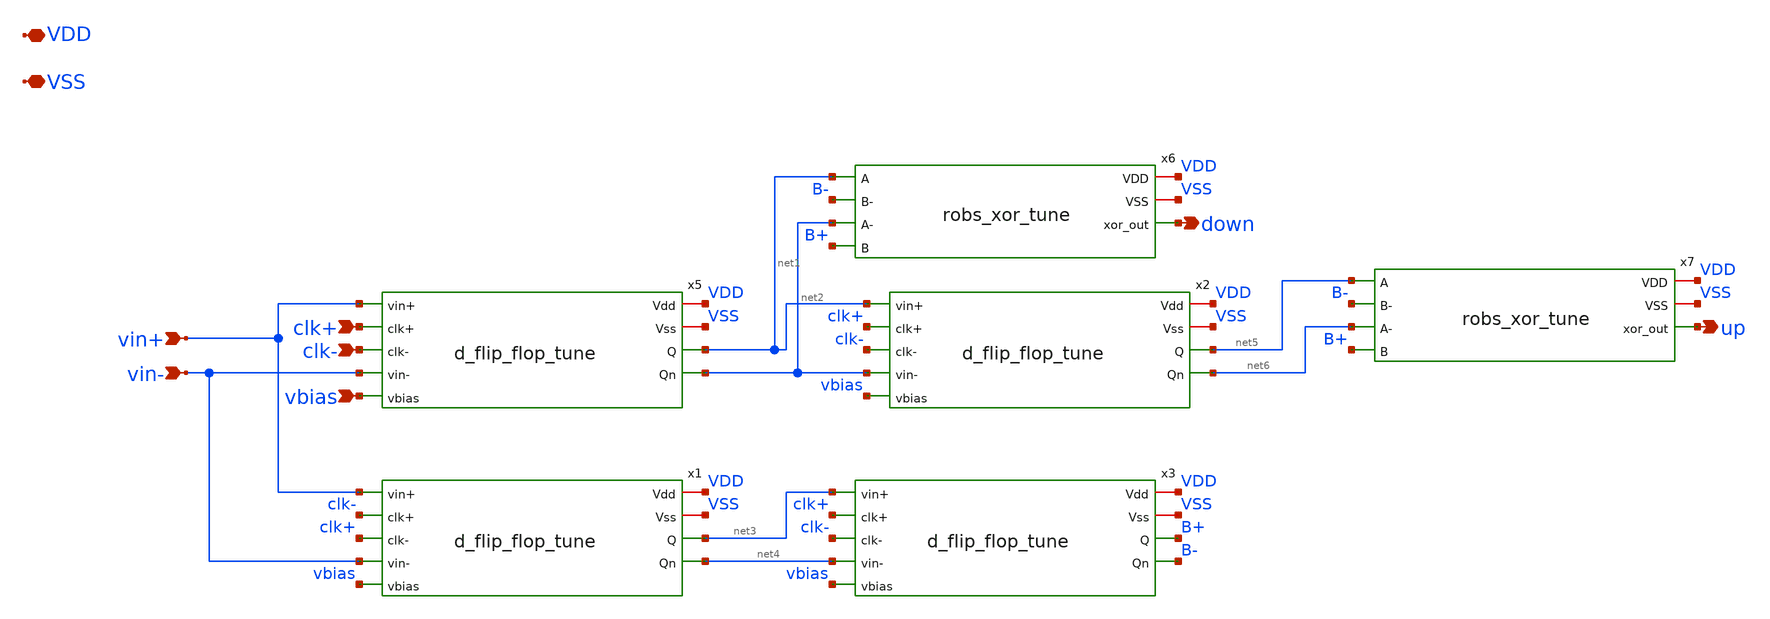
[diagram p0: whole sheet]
** sch_path: xschem/tuning/alexander_phase_detector_tune.sch
**.subckt alexander_phase_detector_tune down up vin+ vin- clk+ clk- vbias VDD VSS
*.opin down
*.opin up
*.ipin vin+
*.ipin vin-
*.ipin clk+
*.ipin clk-
*.ipin vbias
*.iopin VDD
*.iopin VSS
x6 net1 VDD B- VSS down net2 B+ robs_xor_tune
x7 net5 VDD B- VSS up net6 B+ robs_xor_tune
x5 VDD VSS net1 net2 vin+ clk+ clk- vin- vbias d_flip_flop_tune
x1 VDD VSS net3 net4 vin+ clk- clk+ vin- vbias d_flip_flop_tune
x2 VDD VSS net5 net6 net1 clk+ clk- net2 vbias d_flip_flop_tune
x3 VDD VSS B+ B- net3 clk+ clk- net4 vbias d_flip_flop_tune
**.ends

* expanding   symbol:  robs_xor_tune.sym # of pins=7
** sym_path: xschem/tuning/robs_xor_tune.sym
** sch_path: xschem/tuning/robs_xor_tune.sch
.subckt robs_xor_tune A VDD B- VSS xor_out A- B
*.opin xor_out
*.ipin A
*.ipin B-
*.ipin A-
*.ipin B
*.iopin VDD
*.iopin VSS
XM5 net1 A VDD VDD sky130_fd_pr__pfet_01v8 L=0.15 W=2 nf=1 ad='int((nf+1)/2) * W/nf * 0.29' as='int((nf+2)/2) * W/nf * 0.29'
+ pd='2*int((nf+1)/2) * (W/nf + 0.29)' ps='2*int((nf+2)/2) * (W/nf + 0.29)' nrd='0.29 / W' nrs='0.29 / W'
+ sa=0 sb=0 sd=0 mult=1 m=1
XM6 xor_out A- net3 VSS sky130_fd_pr__nfet_01v8 L=0.15 W=2 nf=1 ad='int((nf+1)/2) * W/nf * 0.29' as='int((nf+2)/2) * W/nf * 0.29'
+ pd='2*int((nf+1)/2) * (W/nf + 0.29)' ps='2*int((nf+2)/2) * (W/nf + 0.29)' nrd='0.29 / W' nrs='0.29 / W'
+ sa=0 sb=0 sd=0 mult=1 m=1
XM1 xor_out B- net1 VDD sky130_fd_pr__pfet_01v8 L=0.15 W=2 nf=1 ad='int((nf+1)/2) * W/nf * 0.29' as='int((nf+2)/2) * W/nf * 0.29'
+ pd='2*int((nf+1)/2) * (W/nf + 0.29)' ps='2*int((nf+2)/2) * (W/nf + 0.29)' nrd='0.29 / W' nrs='0.29 / W'
+ sa=0 sb=0 sd=0 mult=1 m=1
XM2 net2 A- VDD VDD sky130_fd_pr__pfet_01v8 L=0.15 W=2 nf=1 ad='int((nf+1)/2) * W/nf * 0.29' as='int((nf+2)/2) * W/nf * 0.29'
+ pd='2*int((nf+1)/2) * (W/nf + 0.29)' ps='2*int((nf+2)/2) * (W/nf + 0.29)' nrd='0.29 / W' nrs='0.29 / W'
+ sa=0 sb=0 sd=0 mult=1 m=1
XM3 xor_out B net2 VDD sky130_fd_pr__pfet_01v8 L=0.15 W=2 nf=1 ad='int((nf+1)/2) * W/nf * 0.29' as='int((nf+2)/2) * W/nf * 0.29'
+ pd='2*int((nf+1)/2) * (W/nf + 0.29)' ps='2*int((nf+2)/2) * (W/nf + 0.29)' nrd='0.29 / W' nrs='0.29 / W'
+ sa=0 sb=0 sd=0 mult=1 m=1
XM4 net3 B- VSS VSS sky130_fd_pr__nfet_01v8 L=0.15 W=2 nf=1 ad='int((nf+1)/2) * W/nf * 0.29' as='int((nf+2)/2) * W/nf * 0.29'
+ pd='2*int((nf+1)/2) * (W/nf + 0.29)' ps='2*int((nf+2)/2) * (W/nf + 0.29)' nrd='0.29 / W' nrs='0.29 / W'
+ sa=0 sb=0 sd=0 mult=1 m=1
XM7 xor_out A net4 VSS sky130_fd_pr__nfet_01v8 L=0.15 W=2 nf=1 ad='int((nf+1)/2) * W/nf * 0.29' as='int((nf+2)/2) * W/nf * 0.29'
+ pd='2*int((nf+1)/2) * (W/nf + 0.29)' ps='2*int((nf+2)/2) * (W/nf + 0.29)' nrd='0.29 / W' nrs='0.29 / W'
+ sa=0 sb=0 sd=0 mult=1 m=1
XM8 net4 B VSS VSS sky130_fd_pr__nfet_01v8 L=0.15 W=2 nf=1 ad='int((nf+1)/2) * W/nf * 0.29' as='int((nf+2)/2) * W/nf * 0.29'
+ pd='2*int((nf+1)/2) * (W/nf + 0.29)' ps='2*int((nf+2)/2) * (W/nf + 0.29)' nrd='0.29 / W' nrs='0.29 / W'
+ sa=0 sb=0 sd=0 mult=1 m=1
.ends


* expanding   symbol:  d_flip_flop_tune.sym # of pins=9
** sym_path: xschem/tuning/d_flip_flop_tune.sym
** sch_path: xschem/tuning/d_flip_flop_tune.sch
.subckt d_flip_flop_tune Vdd Vss Q Qn vin+ clk+ clk- vin- vbias
*.opin Qn
*.opin Q
*.ipin vin+
*.ipin vin-
*.ipin clk+
*.ipin clk-
*.ipin vbias
*.iopin Vdd
*.iopin Vss
x1 net1 net2 vin+ vin- Vdd Vss clk- clk+ vbias d_latch_tune
x2 Q Qn net1 net2 Vdd Vss clk+ clk- vbias d_latch_tune
.ends


* expanding   symbol:  d_latch_tune.sym # of pins=9
** sym_path: xschem/tuning/d_latch_tune.sym
** sch_path: xschem/tuning/d_latch_tune.sch
.subckt d_latch_tune vout+ vout- vin+ vin- VDD VSS clk+ clk- vbias
*.iopin VDD
*.iopin VSS
*.ipin vin+
*.ipin clk-
*.ipin vbias
*.opin vout+
*.ipin clk+
*.opin vout-
*.ipin vin-
XM1 net1 vin+ net3 VSS sky130_fd_pr__nfet_01v8 L=0.15 W=5 nf=1 ad='int((nf+1)/2) * W/nf * 0.29' as='int((nf+2)/2) * W/nf * 0.29'
+ pd='2*int((nf+1)/2) * (W/nf + 0.29)' ps='2*int((nf+2)/2) * (W/nf + 0.29)' nrd='0.29 / W' nrs='0.29 / W'
+ sa=0 sb=0 sd=0 mult=1 m=1
XM2 net4 vbias VSS VSS sky130_fd_pr__nfet_01v8 L=0.15 W=8 nf=1 ad='int((nf+1)/2) * W/nf * 0.29' as='int((nf+2)/2) * W/nf * 0.29'
+ pd='2*int((nf+1)/2) * (W/nf + 0.29)' ps='2*int((nf+2)/2) * (W/nf + 0.29)' nrd='0.29 / W' nrs='0.29 / W'
+ sa=0 sb=0 sd=0 mult=1 m=1
XM4 net2 vin- net3 VSS sky130_fd_pr__nfet_01v8 L=0.15 W=5 nf=1 ad='int((nf+1)/2) * W/nf * 0.29' as='int((nf+2)/2) * W/nf * 0.29'
+ pd='2*int((nf+1)/2) * (W/nf + 0.29)' ps='2*int((nf+2)/2) * (W/nf + 0.29)' nrd='0.29 / W' nrs='0.29 / W'
+ sa=0 sb=0 sd=0 mult=1 m=1
XM3 net2 net1 net5 VSS sky130_fd_pr__nfet_01v8 L=0.15 W=5 nf=1 ad='int((nf+1)/2) * W/nf * 0.29' as='int((nf+2)/2) * W/nf * 0.29'
+ pd='2*int((nf+1)/2) * (W/nf + 0.29)' ps='2*int((nf+2)/2) * (W/nf + 0.29)' nrd='0.29 / W' nrs='0.29 / W'
+ sa=0 sb=0 sd=0 mult=1 m=1
XM5 net1 net2 net5 VSS sky130_fd_pr__nfet_01v8 L=0.15 W=5 nf=1 ad='int((nf+1)/2) * W/nf * 0.29' as='int((nf+2)/2) * W/nf * 0.29'
+ pd='2*int((nf+1)/2) * (W/nf + 0.29)' ps='2*int((nf+2)/2) * (W/nf + 0.29)' nrd='0.29 / W' nrs='0.29 / W'
+ sa=0 sb=0 sd=0 mult=1 m=1
XM6 net3 clk+ net4 VSS sky130_fd_pr__nfet_01v8 L=0.15 W=5 nf=1 ad='int((nf+1)/2) * W/nf * 0.29' as='int((nf+2)/2) * W/nf * 0.29'
+ pd='2*int((nf+1)/2) * (W/nf + 0.29)' ps='2*int((nf+2)/2) * (W/nf + 0.29)' nrd='0.29 / W' nrs='0.29 / W'
+ sa=0 sb=0 sd=0 mult=1 m=1
XM7 net5 clk- net4 VSS sky130_fd_pr__nfet_01v8 L=0.15 W=5 nf=1 ad='int((nf+1)/2) * W/nf * 0.29' as='int((nf+2)/2) * W/nf * 0.29'
+ pd='2*int((nf+1)/2) * (W/nf + 0.29)' ps='2*int((nf+2)/2) * (W/nf + 0.29)' nrd='0.29 / W' nrs='0.29 / W'
+ sa=0 sb=0 sd=0 mult=1 m=1
XM8 vout+ net1 VDD VDD sky130_fd_pr__pfet_01v8 L=0.15 W=3 nf=1 ad='int((nf+1)/2) * W/nf * 0.29' as='int((nf+2)/2) * W/nf * 0.29'
+ pd='2*int((nf+1)/2) * (W/nf + 0.29)' ps='2*int((nf+2)/2) * (W/nf + 0.29)' nrd='0.29 / W' nrs='0.29 / W'
+ sa=0 sb=0 sd=0 mult=1 m=1
XM9 vout+ net1 VSS VSS sky130_fd_pr__nfet_01v8 L=0.15 W=1 nf=1 ad='int((nf+1)/2) * W/nf * 0.29' as='int((nf+2)/2) * W/nf * 0.29'
+ pd='2*int((nf+1)/2) * (W/nf + 0.29)' ps='2*int((nf+2)/2) * (W/nf + 0.29)' nrd='0.29 / W' nrs='0.29 / W'
+ sa=0 sb=0 sd=0 mult=1 m=1
XM10 vout- net2 VDD VDD sky130_fd_pr__pfet_01v8 L=0.15 W=3 nf=1 ad='int((nf+1)/2) * W/nf * 0.29' as='int((nf+2)/2) * W/nf * 0.29'
+ pd='2*int((nf+1)/2) * (W/nf + 0.29)' ps='2*int((nf+2)/2) * (W/nf + 0.29)' nrd='0.29 / W' nrs='0.29 / W'
+ sa=0 sb=0 sd=0 mult=1 m=1
XM11 vout- net2 VSS VSS sky130_fd_pr__nfet_01v8 L=0.15 W=1 nf=1 ad='int((nf+1)/2) * W/nf * 0.29' as='int((nf+2)/2) * W/nf * 0.29'
+ pd='2*int((nf+1)/2) * (W/nf + 0.29)' ps='2*int((nf+2)/2) * (W/nf + 0.29)' nrd='0.29 / W' nrs='0.29 / W'
+ sa=0 sb=0 sd=0 mult=1 m=1
XR3 net1 VDD VSS sky130_fd_pr__res_high_po_0p69 L=7 mult=1 m=1
XR1 net2 VDD VSS sky130_fd_pr__res_high_po_0p69 L=7 mult=1 m=1
.ends

.end
